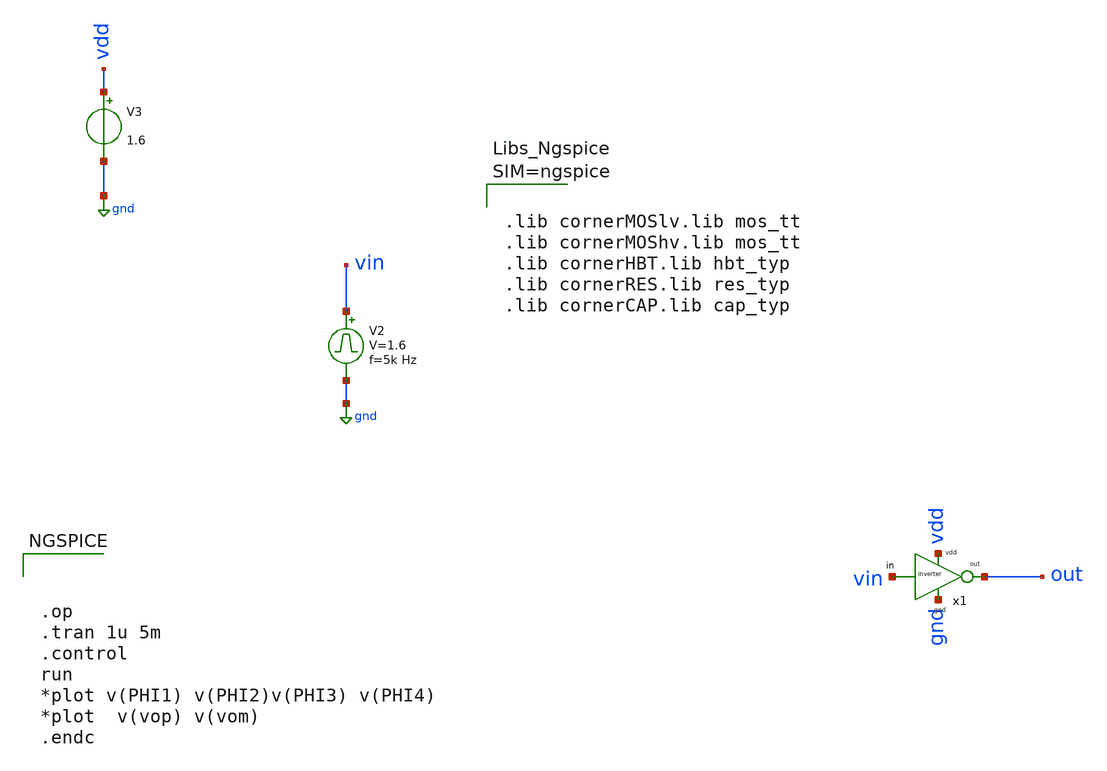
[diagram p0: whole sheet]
** sch_path: dependencies/OTA/OTA-main/schematic/xschem/temp.sch
**.subckt temp
V2 vin gnd pulse 0 1.6 '0.495/ 5k ' '0.01/5k ' '0.01/5k ' '0.49/5k ' '1/5k '
V3 vdd gnd 1.6
x1 vin out vdd gnd inverter
**** begin user architecture code



.lib cornerMOSlv.lib mos_tt
.lib cornerMOShv.lib mos_tt
.lib cornerHBT.lib hbt_typ
.lib cornerRES.lib res_typ
.lib cornerCAP.lib cap_typ






.op
.tran 1u 5m
.control
run
*plot v(PHI1) v(PHI2)v(PHI3) v(PHI4)
*plot  v(vop) v(vom)
.endc


**** end user architecture code
**.ends

* expanding   symbol:
*+  /home/designer/shared/unicass_2026/Design_Files/github_clone_circuit_/UNI-CASS_Project_2025_IIT_DH/Clock_gen_using_transistor_hv/inverter.sym # of pins=4
** sym_path: /home/designer/shared/unicass_2026/Design_Files/github_clone_circuit_/UNI-CASS_Project_2025_IIT_DH/Clock_gen_using_transistor_hv/inverter.sym
** sch_path: /home/designer/shared/unicass_2026/Design_Files/github_clone_circuit_/UNI-CASS_Project_2025_IIT_DH/Clock_gen_using_transistor_hv/inverter.sch
.subckt inverter in out vdd gnd
*.iopin in
*.iopin vdd
*.iopin out
*.iopin gnd
XM3 out in vdd vdd sg13_hv_pmos w=0.6u l=0.9u ng=1 m=1 mm_ok=1
XM1 out in gnd gnd sg13_hv_nmos w=0.3u l=0.45u ng=1 m=1 mm_ok=1
.ends

.GLOBAL gnd
.end
